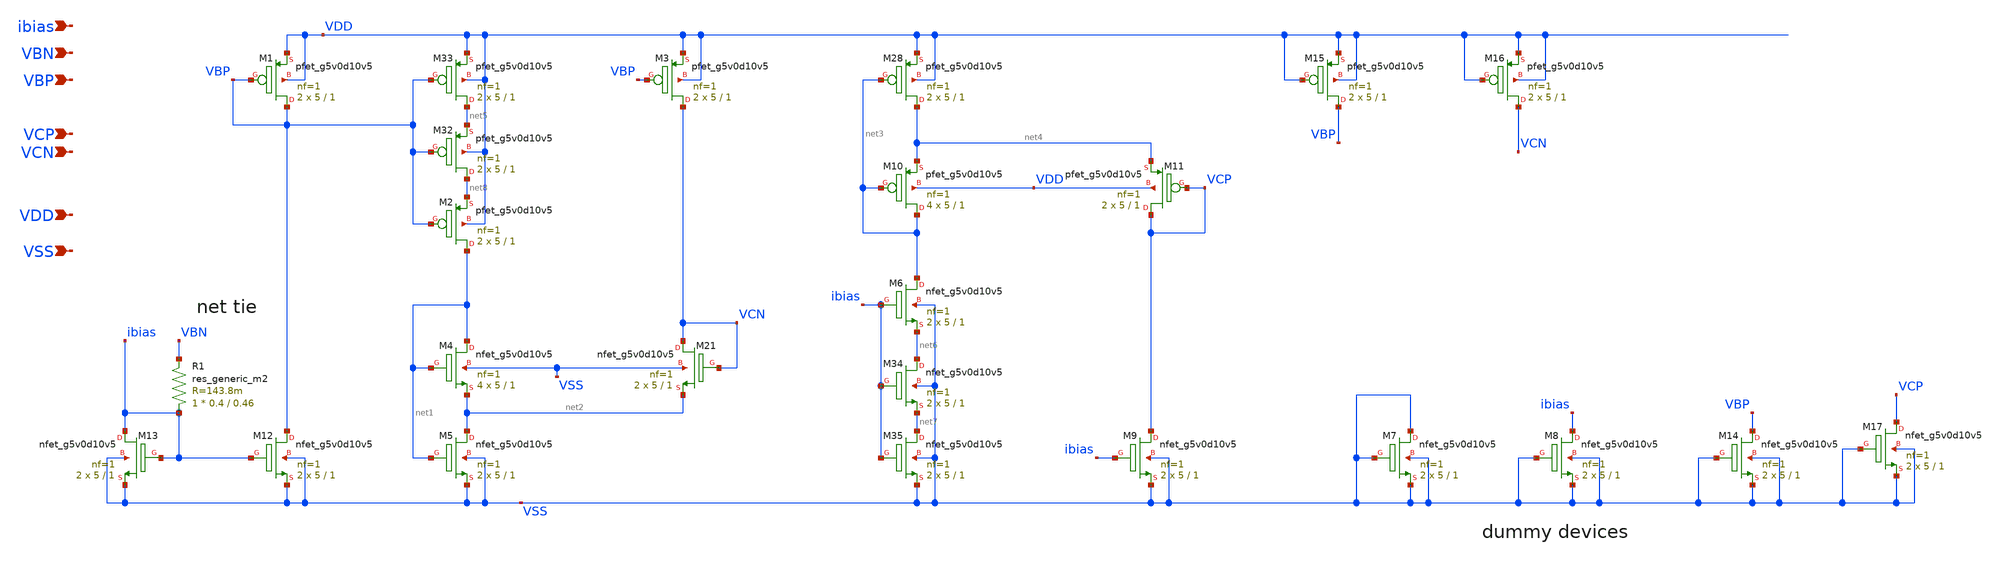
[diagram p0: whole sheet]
** sch_path: images/foss-asic-tools/addons/examples/open-pmic/design/bias-circuit/cascode_bias.sch
**.subckt cascode_bias ibias VBN VBP VCP VCN VDD VSS
*.ipin ibias
*.ipin VBN
*.ipin VBP
*.ipin VCP
*.ipin VCN
*.ipin VDD
*.ipin VSS
XM2 net1 VBP net8 VDD sky130_fd_pr__pfet_g5v0d10v5 L=1 W=5 nf=1 ad='int((nf+1)/2) * W/nf * 0.29' as='int((nf+2)/2) * W/nf * 0.29'
+ pd='2*int((nf+1)/2) * (W/nf + 0.29)' ps='2*int((nf+2)/2) * (W/nf + 0.29)' nrd='0.29 / W' nrs='0.29 / W'
+ sa=0 sb=0 sd=0 mult=2 m=2
XM3 VCN VBP VDD VDD sky130_fd_pr__pfet_g5v0d10v5 L=1 W=5 nf=1 ad='int((nf+1)/2) * W/nf * 0.29' as='int((nf+2)/2) * W/nf * 0.29'
+ pd='2*int((nf+1)/2) * (W/nf + 0.29)' ps='2*int((nf+2)/2) * (W/nf + 0.29)' nrd='0.29 / W' nrs='0.29 / W'
+ sa=0 sb=0 sd=0 mult=2 m=2
XM4 net1 net1 net2 VSS sky130_fd_pr__nfet_g5v0d10v5 L=1 W=5 nf=1 ad='int((nf+1)/2) * W/nf * 0.29' as='int((nf+2)/2) * W/nf * 0.29'
+ pd='2*int((nf+1)/2) * (W/nf + 0.29)' ps='2*int((nf+2)/2) * (W/nf + 0.29)' nrd='0.29 / W' nrs='0.29 / W'
+ sa=0 sb=0 sd=0 mult=4 m=4
XM5 net2 net1 VSS VSS sky130_fd_pr__nfet_g5v0d10v5 L=1 W=5 nf=1 ad='int((nf+1)/2) * W/nf * 0.29' as='int((nf+2)/2) * W/nf * 0.29'
+ pd='2*int((nf+1)/2) * (W/nf + 0.29)' ps='2*int((nf+2)/2) * (W/nf + 0.29)' nrd='0.29 / W' nrs='0.29 / W'
+ sa=0 sb=0 sd=0 mult=2 m=2
XM21 VCN VCN net2 VSS sky130_fd_pr__nfet_g5v0d10v5 L=1 W=5 nf=1 ad='int((nf+1)/2) * W/nf * 0.29' as='int((nf+2)/2) * W/nf * 0.29'
+ pd='2*int((nf+1)/2) * (W/nf + 0.29)' ps='2*int((nf+2)/2) * (W/nf + 0.29)' nrd='0.29 / W' nrs='0.29 / W'
+ sa=0 sb=0 sd=0 mult=2 m=2
XM6 net3 ibias net6 VSS sky130_fd_pr__nfet_g5v0d10v5 L=1 W=5 nf=1 ad='int((nf+1)/2) * W/nf * 0.29' as='int((nf+2)/2) * W/nf * 0.29'
+ pd='2*int((nf+1)/2) * (W/nf + 0.29)' ps='2*int((nf+2)/2) * (W/nf + 0.29)' nrd='0.29 / W' nrs='0.29 / W'
+ sa=0 sb=0 sd=0 mult=2 m=2
XM9 VCP ibias VSS VSS sky130_fd_pr__nfet_g5v0d10v5 L=1 W=5 nf=1 ad='int((nf+1)/2) * W/nf * 0.29' as='int((nf+2)/2) * W/nf * 0.29'
+ pd='2*int((nf+1)/2) * (W/nf + 0.29)' ps='2*int((nf+2)/2) * (W/nf + 0.29)' nrd='0.29 / W' nrs='0.29 / W'
+ sa=0 sb=0 sd=0 mult=2 m=2
XM10 net3 net3 net4 VDD sky130_fd_pr__pfet_g5v0d10v5 L=1 W=5 nf=1 ad='int((nf+1)/2) * W/nf * 0.29' as='int((nf+2)/2) * W/nf * 0.29'
+ pd='2*int((nf+1)/2) * (W/nf + 0.29)' ps='2*int((nf+2)/2) * (W/nf + 0.29)' nrd='0.29 / W' nrs='0.29 / W'
+ sa=0 sb=0 sd=0 mult=4 m=4
XM11 VCP VCP net4 VDD sky130_fd_pr__pfet_g5v0d10v5 L=1 W=5 nf=1 ad='int((nf+1)/2) * W/nf * 0.29' as='int((nf+2)/2) * W/nf * 0.29'
+ pd='2*int((nf+1)/2) * (W/nf + 0.29)' ps='2*int((nf+2)/2) * (W/nf + 0.29)' nrd='0.29 / W' nrs='0.29 / W'
+ sa=0 sb=0 sd=0 mult=2 m=2
XM28 net4 net3 VDD VDD sky130_fd_pr__pfet_g5v0d10v5 L=1 W=5 nf=1 ad='int((nf+1)/2) * W/nf * 0.29' as='int((nf+2)/2) * W/nf * 0.29'
+ pd='2*int((nf+1)/2) * (W/nf + 0.29)' ps='2*int((nf+2)/2) * (W/nf + 0.29)' nrd='0.29 / W' nrs='0.29 / W'
+ sa=0 sb=0 sd=0 mult=2 m=2
XM12 VBP ibias VSS VSS sky130_fd_pr__nfet_g5v0d10v5 L=1 W=5 nf=1 ad='int((nf+1)/2) * W/nf * 0.29' as='int((nf+2)/2) * W/nf * 0.29'
+ pd='2*int((nf+1)/2) * (W/nf + 0.29)' ps='2*int((nf+2)/2) * (W/nf + 0.29)' nrd='0.29 / W' nrs='0.29 / W'
+ sa=0 sb=0 sd=0 mult=2 m=2
XM32 net8 VBP net5 VDD sky130_fd_pr__pfet_g5v0d10v5 L=1 W=5 nf=1 ad='int((nf+1)/2) * W/nf * 0.29' as='int((nf+2)/2) * W/nf * 0.29'
+ pd='2*int((nf+1)/2) * (W/nf + 0.29)' ps='2*int((nf+2)/2) * (W/nf + 0.29)' nrd='0.29 / W' nrs='0.29 / W'
+ sa=0 sb=0 sd=0 mult=2 m=2
XM33 net5 VBP VDD VDD sky130_fd_pr__pfet_g5v0d10v5 L=1 W=5 nf=1 ad='int((nf+1)/2) * W/nf * 0.29' as='int((nf+2)/2) * W/nf * 0.29'
+ pd='2*int((nf+1)/2) * (W/nf + 0.29)' ps='2*int((nf+2)/2) * (W/nf + 0.29)' nrd='0.29 / W' nrs='0.29 / W'
+ sa=0 sb=0 sd=0 mult=2 m=2
XM34 net6 ibias net7 VSS sky130_fd_pr__nfet_g5v0d10v5 L=1 W=5 nf=1 ad='int((nf+1)/2) * W/nf * 0.29' as='int((nf+2)/2) * W/nf * 0.29'
+ pd='2*int((nf+1)/2) * (W/nf + 0.29)' ps='2*int((nf+2)/2) * (W/nf + 0.29)' nrd='0.29 / W' nrs='0.29 / W'
+ sa=0 sb=0 sd=0 mult=2 m=2
XM35 net7 ibias VSS VSS sky130_fd_pr__nfet_g5v0d10v5 L=1 W=5 nf=1 ad='int((nf+1)/2) * W/nf * 0.29' as='int((nf+2)/2) * W/nf * 0.29'
+ pd='2*int((nf+1)/2) * (W/nf + 0.29)' ps='2*int((nf+2)/2) * (W/nf + 0.29)' nrd='0.29 / W' nrs='0.29 / W'
+ sa=0 sb=0 sd=0 mult=2 m=2
XM13 ibias ibias VSS VSS sky130_fd_pr__nfet_g5v0d10v5 L=1 W=5 nf=1 ad='int((nf+1)/2) * W/nf * 0.29' as='int((nf+2)/2) * W/nf * 0.29'
+ pd='2*int((nf+1)/2) * (W/nf + 0.29)' ps='2*int((nf+2)/2) * (W/nf + 0.29)' nrd='0.29 / W' nrs='0.29 / W'
+ sa=0 sb=0 sd=0 mult=2 m=2
XM1 VBP VBP VDD VDD sky130_fd_pr__pfet_g5v0d10v5 L=1 W=5 nf=1 ad='int((nf+1)/2) * W/nf * 0.29' as='int((nf+2)/2) * W/nf * 0.29'
+ pd='2*int((nf+1)/2) * (W/nf + 0.29)' ps='2*int((nf+2)/2) * (W/nf + 0.29)' nrd='0.29 / W' nrs='0.29 / W'
+ sa=0 sb=0 sd=0 mult=2 m=2
R1 ibias VBN sky130_fd_pr__res_generic_m2 W=0.4 L=0.46 m=1
XM7 VSS VSS VSS VSS sky130_fd_pr__nfet_g5v0d10v5 L=1 W=5 nf=1 ad='int((nf+1)/2) * W/nf * 0.29' as='int((nf+2)/2) * W/nf * 0.29'
+ pd='2*int((nf+1)/2) * (W/nf + 0.29)' ps='2*int((nf+2)/2) * (W/nf + 0.29)' nrd='0.29 / W' nrs='0.29 / W'
+ sa=0 sb=0 sd=0 mult=2 m=2
XM8 ibias VSS VSS VSS sky130_fd_pr__nfet_g5v0d10v5 L=1 W=5 nf=1 ad='int((nf+1)/2) * W/nf * 0.29' as='int((nf+2)/2) * W/nf * 0.29'
+ pd='2*int((nf+1)/2) * (W/nf + 0.29)' ps='2*int((nf+2)/2) * (W/nf + 0.29)' nrd='0.29 / W' nrs='0.29 / W'
+ sa=0 sb=0 sd=0 mult=2 m=2
XM14 VBP VSS VSS VSS sky130_fd_pr__nfet_g5v0d10v5 L=1 W=5 nf=1 ad='int((nf+1)/2) * W/nf * 0.29' as='int((nf+2)/2) * W/nf * 0.29'
+ pd='2*int((nf+1)/2) * (W/nf + 0.29)' ps='2*int((nf+2)/2) * (W/nf + 0.29)' nrd='0.29 / W' nrs='0.29 / W'
+ sa=0 sb=0 sd=0 mult=2 m=2
XM15 VBP VDD VDD VDD sky130_fd_pr__pfet_g5v0d10v5 L=1 W=5 nf=1 ad='int((nf+1)/2) * W/nf * 0.29' as='int((nf+2)/2) * W/nf * 0.29'
+ pd='2*int((nf+1)/2) * (W/nf + 0.29)' ps='2*int((nf+2)/2) * (W/nf + 0.29)' nrd='0.29 / W' nrs='0.29 / W'
+ sa=0 sb=0 sd=0 mult=2 m=2
XM16 VCN VDD VDD VDD sky130_fd_pr__pfet_g5v0d10v5 L=1 W=5 nf=1 ad='int((nf+1)/2) * W/nf * 0.29' as='int((nf+2)/2) * W/nf * 0.29'
+ pd='2*int((nf+1)/2) * (W/nf + 0.29)' ps='2*int((nf+2)/2) * (W/nf + 0.29)' nrd='0.29 / W' nrs='0.29 / W'
+ sa=0 sb=0 sd=0 mult=2 m=2
XM17 VCP VSS VSS VSS sky130_fd_pr__nfet_g5v0d10v5 L=1 W=5 nf=1 ad='int((nf+1)/2) * W/nf * 0.29' as='int((nf+2)/2) * W/nf * 0.29'
+ pd='2*int((nf+1)/2) * (W/nf + 0.29)' ps='2*int((nf+2)/2) * (W/nf + 0.29)' nrd='0.29 / W' nrs='0.29 / W'
+ sa=0 sb=0 sd=0 mult=2 m=2
**.ends
.end
